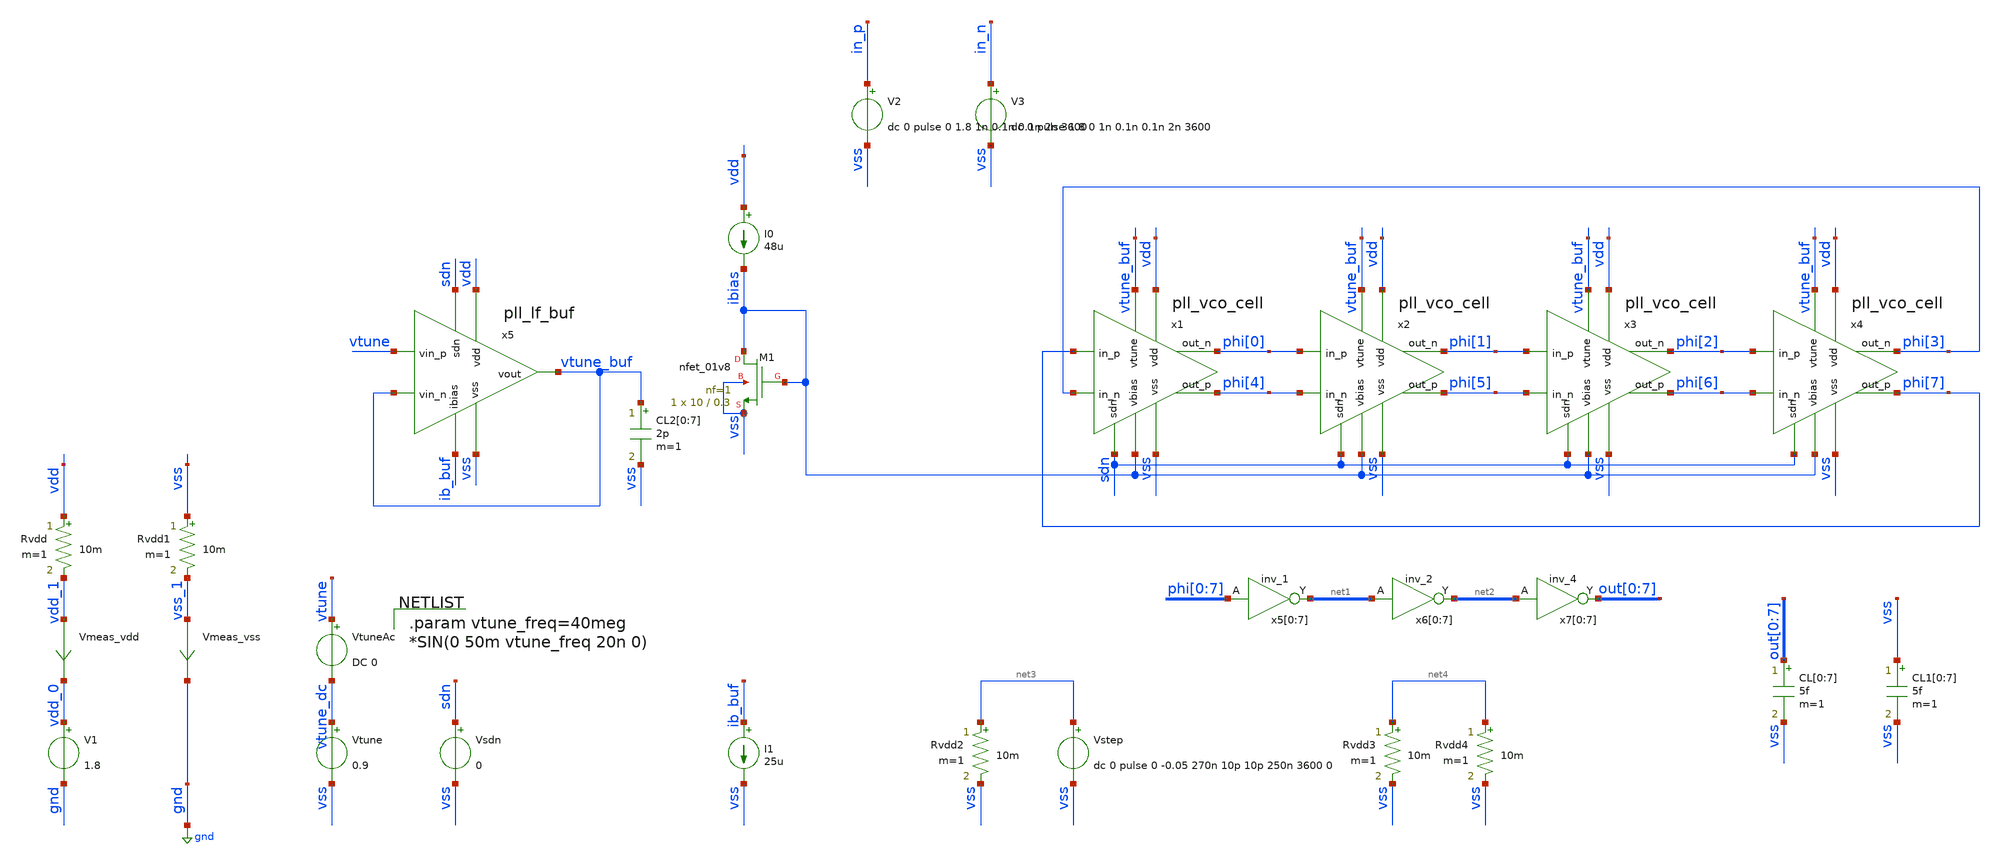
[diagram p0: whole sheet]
** sch_path: pll/pll_vco_cell/simulation/pll_vco_cell_tb.sch
**.subckt pll_vco_cell_tb
V1 vdd_0 gnd 1.8
I0 vdd ibias 48u
Vmeas_vdd vdd_1 vdd_0 0
.save i(vmeas_vdd)
Vtune vtune_dc vss 0.9
V2 in_p vss dc 0 pulse 0 1.8 1n 0.1n 0.1n 2n 3600
V3 in_n vss dc 0 pulse 1.8 0 1n 0.1n 0.1n 2n 3600
XM1 ibias ibias vss vss sky130_fd_pr__nfet_01v8 L=0.3 W=10 nf=1 ad='int((nf+1)/2) * W/nf * 0.29' as='int((nf+2)/2) * W/nf * 0.29'
+ pd='2*int((nf+1)/2) * (W/nf + 0.29)' ps='2*int((nf+2)/2) * (W/nf + 0.29)' nrd='0.29 / W' nrs='0.29 / W'
+ sa=0 sb=0 sd=0 mult=1 m=1
Vsdn sdn vss 0
x5[0] phi[0] vss vss vdd vdd net1[7] sky130_fd_sc_hs__inv_1
x5[1] phi[1] vss vss vdd vdd net1[6] sky130_fd_sc_hs__inv_1
x5[2] phi[2] vss vss vdd vdd net1[5] sky130_fd_sc_hs__inv_1
x5[3] phi[3] vss vss vdd vdd net1[4] sky130_fd_sc_hs__inv_1
x5[4] phi[4] vss vss vdd vdd net1[3] sky130_fd_sc_hs__inv_1
x5[5] phi[5] vss vss vdd vdd net1[2] sky130_fd_sc_hs__inv_1
x5[6] phi[6] vss vss vdd vdd net1[1] sky130_fd_sc_hs__inv_1
x5[7] phi[7] vss vss vdd vdd net1[0] sky130_fd_sc_hs__inv_1
x6[0] net1[7] vss vss vdd vdd net2[7] sky130_fd_sc_hs__inv_2
x6[1] net1[6] vss vss vdd vdd net2[6] sky130_fd_sc_hs__inv_2
x6[2] net1[5] vss vss vdd vdd net2[5] sky130_fd_sc_hs__inv_2
x6[3] net1[4] vss vss vdd vdd net2[4] sky130_fd_sc_hs__inv_2
x6[4] net1[3] vss vss vdd vdd net2[3] sky130_fd_sc_hs__inv_2
x6[5] net1[2] vss vss vdd vdd net2[2] sky130_fd_sc_hs__inv_2
x6[6] net1[1] vss vss vdd vdd net2[1] sky130_fd_sc_hs__inv_2
x6[7] net1[0] vss vss vdd vdd net2[0] sky130_fd_sc_hs__inv_2
x7[0] net2[7] vss vss vdd vdd out[0] sky130_fd_sc_hs__inv_4
x7[1] net2[6] vss vss vdd vdd out[1] sky130_fd_sc_hs__inv_4
x7[2] net2[5] vss vss vdd vdd out[2] sky130_fd_sc_hs__inv_4
x7[3] net2[4] vss vss vdd vdd out[3] sky130_fd_sc_hs__inv_4
x7[4] net2[3] vss vss vdd vdd out[4] sky130_fd_sc_hs__inv_4
x7[5] net2[2] vss vss vdd vdd out[5] sky130_fd_sc_hs__inv_4
x7[6] net2[1] vss vss vdd vdd out[6] sky130_fd_sc_hs__inv_4
x7[7] net2[0] vss vss vdd vdd out[7] sky130_fd_sc_hs__inv_4
CL[0] out[0] vss 5f m=1
CL[1] out[1] vss 5f m=1
CL[2] out[2] vss 5f m=1
CL[3] out[3] vss 5f m=1
CL[4] out[4] vss 5f m=1
CL[5] out[5] vss 5f m=1
CL[6] out[6] vss 5f m=1
CL[7] out[7] vss 5f m=1
Vmeas_vss vss_1 gnd 0
.save i(vmeas_vss)
Rvdd vdd vdd_1 10m m=1
Rvdd1 vss vss_1 10m m=1
CL1[0] vss vss 5f m=1
CL1[1] vss vss 5f m=1
CL1[2] vss vss 5f m=1
CL1[3] vss vss 5f m=1
CL1[4] vss vss 5f m=1
CL1[5] vss vss 5f m=1
CL1[6] vss vss 5f m=1
CL1[7] vss vss 5f m=1
VtuneAc vtune vtune_dc DC 0
Rvdd2 net3 vss 10m m=1
Vstep net3 vss dc 0 pulse 0 -0.05 270n 10p 10p 250n 3600 0
Rvdd3 net4 vss 10m m=1
Rvdd4 net4 vss 10m m=1
I1 ib_buf vss 25u
x1 phi[0] phi[4] phi[7] phi[3] vdd vtune_buf ibias vss sdn pll_vco_cell
x2 phi[1] phi[5] phi[0] phi[4] vdd vtune_buf ibias vss sdn pll_vco_cell
x3 phi[2] phi[6] phi[1] phi[5] vdd vtune_buf ibias vss sdn pll_vco_cell
x4 phi[3] phi[7] phi[2] phi[6] vdd vtune_buf ibias vss sdn pll_vco_cell
x5 vdd vtune sdn vtune_buf vtune_buf ib_buf vss pll_lf_buf
CL2[0] vtune_buf vss 2p m=1
CL2[1] vtune_buf vss 2p m=1
CL2[2] vtune_buf vss 2p m=1
CL2[3] vtune_buf vss 2p m=1
CL2[4] vtune_buf vss 2p m=1
CL2[5] vtune_buf vss 2p m=1
CL2[6] vtune_buf vss 2p m=1
CL2[7] vtune_buf vss 2p m=1
**** begin user architecture code



*.option savecurrents
*.option rshunt = 1e12
*.option gmin = 1e-24

** Settings for PSS osciallator
*.option reltol=1e-5
*.option vntol=3e-8
*.option abstol=1e-13
**.option chgtol=1e-12
*.option trtol=10
.option method=gear



* Set Oscillator nodes to initial conditions to start oscilation
*.ic v("phi<0>")=1.8 v("phi<4>")=0.0 v("phi<1>")=0.0 v("phi<5>")=1.8

.control

* #################################################################
* #
* #                         OPERATING POINT
* #
* #################################################################
reset
save all

* Bias transistor OP params
save i(@m.xm1.msky130_fd_pr__nfet_01v8[id])
save @m.xm1.msky130_fd_pr__nfet_01v8[gm]
save v(@m.xm1.msky130_fd_pr__nfet_01v8[vds])
save v(@m.xm1.msky130_fd_pr__nfet_01v8[vgs])
save v(@m.xm1.msky130_fd_pr__nfet_01v8[vth])
save v(@m.xm1.msky130_fd_pr__nfet_01v8[vdsat])

* VCO cell OP params
save i(@m.x1.xm1.msky130_fd_pr__nfet_01v8[id])
save @m.x1.xm1.msky130_fd_pr__nfet_01v8[gm]
save v(@m.x1.xm1.msky130_fd_pr__nfet_01v8[vds])
save v(@m.x1.xm1.msky130_fd_pr__nfet_01v8[vgs])
save v(@m.x1.xm1.msky130_fd_pr__nfet_01v8[vth])
save v(@m.x1.xm1.msky130_fd_pr__nfet_01v8[vdsat])

save i(@m.x1.xm2.msky130_fd_pr__nfet_01v8[id])
save @m.x1.xm2.msky130_fd_pr__nfet_01v8[gm]
save v(@m.x1.xm2.msky130_fd_pr__nfet_01v8[vds])
save v(@m.x1.xm2.msky130_fd_pr__nfet_01v8[vgs])
save v(@m.x1.xm2.msky130_fd_pr__nfet_01v8[vth])
save v(@m.x1.xm2.msky130_fd_pr__nfet_01v8[vdsat])

save i(@m.x1.xm3.msky130_fd_pr__nfet_01v8[id])
save @m.x1.xm3.msky130_fd_pr__nfet_01v8[gm]
save v(@m.x1.xm3.msky130_fd_pr__nfet_01v8[vds])
save v(@m.x1.xm3.msky130_fd_pr__nfet_01v8[vgs])
save v(@m.x1.xm3.msky130_fd_pr__nfet_01v8[vth])
save v(@m.x1.xm3.msky130_fd_pr__nfet_01v8[vdsat])

save i(@m.x1.xm4.msky130_fd_pr__pfet_01v8[id])
save @m.x1.xm4.msky130_fd_pr__pfet_01v8[gm]
save v(@m.x1.xm4.msky130_fd_pr__pfet_01v8[vds])
save v(@m.x1.xm4.msky130_fd_pr__pfet_01v8[vgs])
save v(@m.x1.xm4.msky130_fd_pr__pfet_01v8[vth])
save v(@m.x1.xm4.msky130_fd_pr__pfet_01v8[vdsat])

save i(@m.x1.xm5.msky130_fd_pr__pfet_01v8[id])
save @m.x1.xm5.msky130_fd_pr__pfet_01v8[gm]
save v(@m.x1.xm5.msky130_fd_pr__pfet_01v8[vds])
save v(@m.x1.xm5.msky130_fd_pr__pfet_01v8[vgs])
save v(@m.x1.xm5.msky130_fd_pr__pfet_01v8[vth])
save v(@m.x1.xm5.msky130_fd_pr__pfet_01v8[vdsat])

save i(@m.x1.xm6.msky130_fd_pr__pfet_01v8[id])
save @m.x1.xm6.msky130_fd_pr__pfet_01v8[gm]
save v(@m.x1.xm6.msky130_fd_pr__pfet_01v8[vds])
save v(@m.x1.xm6.msky130_fd_pr__pfet_01v8[vgs])
save v(@m.x1.xm6.msky130_fd_pr__pfet_01v8[vth])
save v(@m.x1.xm6.msky130_fd_pr__pfet_01v8[vdsat])

save i(@m.x1.xm7.msky130_fd_pr__pfet_01v8[id])
save @m.x1.xm7.msky130_fd_pr__pfet_01v8[gm]
save v(@m.x1.xm7.msky130_fd_pr__pfet_01v8[vds])
save v(@m.x1.xm7.msky130_fd_pr__pfet_01v8[vgs])
save v(@m.x1.xm7.msky130_fd_pr__pfet_01v8[vth])
save v(@m.x1.xm7.msky130_fd_pr__pfet_01v8[vdsat])


op
set filetype=binary
write pll_vco_cell_tb.raw all

* #################################################################
* #
* #                 TRANSIENT OSCILATION REGIME
* #
* #################################################################
reset
setplot const
save all
save v(in_p)
save v(in_n)
save v(vtune)
save v(vtune_buf)
save v(vsdn)

*ic v("phi<0>")=1.8 v("phi<4>")=0 v("phi<1>")=0 v("phi<5>")=1.8
tran 0.005n 500n uic
set filetype=ascii
write pll_vco_cell_tb_tran.raw v(vtune) v(vtune_buf) v("out<3>") v("out<7>") v("phi<3>") v("phi<7>")

* Plot internal nodes
*plot v("phi<0>") v("phi<4>")
*plot v("phi<1>") v("phi<5>")

* Plot outputs
plot v("out<0>")+2 v("out<4>")+2 v("out<1>")+0 v("out<5>")+0 v("out<2>")-2 v("out<6>")-2
+ v("out<3>")-4 v("out<7>")-4
plot v("phi<0>")+2 v("phi<4>")+2 v("phi<1>")+0 v("phi<5>")+0 v("phi<2>")-2 v("phi<6>")-2
+ v("phi<3>")-4 v("phi<7>")-4

*plot v("out<0>") v("out<4>")
*plot v("out<1>") v("out<5>")
*plot v("out<2>") v("out<6>")
*plot v("out<3>") v("out<7>")


* #################################################################
* #
* #                 TRANSIENT OSCILATION REGIME
* #
* #################################################################

let run_pss = 0
if run_pss > 0
	echo #############################################################
	echo Initial PSS run
	echo #############################################################

	reset
	setplot const
	save all

	*ic v("phi<0>")=1.8 v("phi<4>")=0 v("phi<1>")=0 v("phi<5>")=1.8
	pss 250e6 40n "out<7>" 128 10 3 100e-3 uic

	set filetype=ascii
	write pll_vco_cell_tb_pss.raw all
end

let run_pss_sweep = 0
if run_pss_sweep > 0
	echo #############################################################
	echo Sweep PSS run
	echo #############################################################

	reset
	setplot const
	save all

	let run = 0
	let vtune_start = 0.0
	let vtune_stop = 1.8
	let vtune_step = 0.01
	let vtune_val = vtune_start
	let vtune_length = (vtune_stop-vtune_start)/vtune_step

	set curplot = new
	set pss_sweep_plot = $curplot

	let fout = vector(vtune_length)
	let vtune_sweep = vector(vtune_length)

	while vtune_val le vtune_stop
		* Print run variables
		set run = $&run
		set run_total = $&vtune_length
		set vtune_val = $&vtune_val
		echo #############################################################
		echo PSS run: $run / $run_total for vtune: $vtune_val V
		echo #############################################################

		* Run Transient
		echo START TRAN
		set dt = $curplot
		reset

		* Set sweep variable
		alter Vtune = vtune_val
		echo 0: $vtune_val

		save vtune "v(out<7>)" "v(out<3>)"
		tran 0.005n 60n uic
		set filetype=ascii
		set tranfilename =  {pll_vco_cell_tb_tran_sweep_}{$&run}{.raw}
		echo $tranfilename
		write $tranfilename vtune "out<7>" "out<3>"
		echo END TRAN
		setplot $dt

		* Execute analysis + set plot environment
		echo START PSS
		reset

		* Set sweep variable
		alter Vtune = vtune_val
		echo Vtune DC: $vtune_val

		save vtune "v(out<7>)" "v(out<3>)"
		pss 200e6 40n "out<7>" 128 10 3 100e-3 uic
		set dt = $curplot
		setplot $pss_sweep_plot


		* Save values to variable
		let vtune_sweep[$run] = vtune_val
		let fout[$run] = {$dt}.frequency[1]

		let fosc=fout[$run]/1e6
		set fosc = $&fosc
		echo Measured Fosc: $fosc MHz

		echo END PSS
		setplot $dt

		let vtune_val = vtune_val + vtune_step
		let run = run + 1

	end
	*plot v({$pss_sweep_plot}.all)
	plot fout vs vtune_sweep

	setplot $pss_sweep_plot
	set filetype=ascii
	write pll_vco_cell_tb_pss_sweep.raw all
end

* #################################################################
* #
* #                 AC RESPONSE SIMULATED IN TRANSIENT
* #
* #################################################################

let run_tran_ac_sweep = 0
if run_tran_ac_sweep > 0
	echo #############################################################
	echo Sweep TRAN AC run
	echo #############################################################

	reset
	setplot const
	save all


	* Setup sweep values
	let vtune_freq_start = 100meg
	let vtune_freq_stop = 10000meg
	let vtune_freq_step = 100
	compose vtune_freq_vect dec=$&vtune_freq_step start=$&vtune_freq_start stop=$&vtune_freq_stop
	let vtune_freq_val = vtune_freq_vect[0]

	* Write frequency vector to file
	set filetype=ascii
	write pll_vco_cell_tb_tran_ac_sweep_input.raw vtune_freq_vect

	* Counter Values
	let run = 0
	let vtune_freq_length = 0
	foreach vtune_freq_val $&vtune_freq_vect
		let vtune_freq_length = vtune_freq_length + 1
	end

	* Setup Plot environment
	set curplot = new
	set tran_ac_sweep_plot = $curplot

	*let fout = vector(vtune_freq_length)
	*let vtune_freq_sweep = vector(vtune_freq_length)

	foreach vtune_freq_val $&vtune_freq_vect
		* Print run variables
		set run = $&run
		set run_total = $&vtune_freq_length
		echo #############################################################
		echo TRAN AC run: $run / $run_total for vtune: $vtune_freq_val Hz
		echo #############################################################

		* Run Transient
		echo START TRAN
		set dt = $curplot

		* Set sweep variable
		alterparam vtune_freq = $vtune_freq_val
		echo Vtune Frequency: $vtune_freq_val

		* Run
		reset
		save vtune vtune_buf "v(out<7>)" "v(out<3>)"
		tran 0.005n 520n uic
		set filetype=ascii
		set tranfilename =  {pll_vco_cell_tb_tran_ac_sweep_}{$&run}{.raw}
		echo $tranfilename
		write $tranfilename vtune "out<7>" "out<3>"
		echo END TRAN
		setplot $dt

		let run = run + 1
	end

	*setplot $pss_sweep_plot
	*set filetype=ascii
	*write pll_vco_cell_tb_pss_sweep.raw all
end


*rusage
.endc



.options wnflag=1
.include $::SKYWATER_MODELS/cells/nfet_01v8/sky130_fd_pr__nfet_01v8__tt.corner.spice
.include $::SKYWATER_MODELS/cells/nfet_01v8_lvt/sky130_fd_pr__nfet_01v8_lvt__tt.corner.spice
.include $::SKYWATER_MODELS/cells/pfet_01v8/sky130_fd_pr__pfet_01v8__tt.corner.spice
.include $::SKYWATER_MODELS/cells/nfet_03v3_nvt/sky130_fd_pr__nfet_03v3_nvt__tt.corner.spice
.include $::SKYWATER_MODELS/cells/nfet_05v0_nvt/sky130_fd_pr__nfet_05v0_nvt__tt.corner.spice
.include $::SKYWATER_MODELS/cells/esd_nfet_01v8/sky130_fd_pr__esd_nfet_01v8__tt.corner.spice
.include $::SKYWATER_MODELS/cells/pfet_01v8_lvt/sky130_fd_pr__pfet_01v8_lvt__tt.corner.spice
.include $::SKYWATER_MODELS/cells/pfet_01v8_hvt/sky130_fd_pr__pfet_01v8_hvt__tt.corner.spice
.include $::SKYWATER_MODELS/cells/esd_pfet_g5v0d10v5/sky130_fd_pr__esd_pfet_g5v0d10v5__tt.corner.spice
.include $::SKYWATER_MODELS/cells/pfet_g5v0d10v5/sky130_fd_pr__pfet_g5v0d10v5__tt.corner.spice
.include $::SKYWATER_MODELS/cells/pfet_g5v0d16v0/sky130_fd_pr__pfet_g5v0d16v0__tt.corner.spice
.include $::SKYWATER_MODELS/cells/nfet_g5v0d10v5/sky130_fd_pr__nfet_g5v0d10v5__tt.corner.spice
.include $::SKYWATER_MODELS/cells/nfet_g5v0d16v0/sky130_fd_pr__nfet_g5v0d16v0__tt_discrete.corner.spice
.include $::SKYWATER_MODELS/cells/esd_nfet_g5v0d10v5/sky130_fd_pr__esd_nfet_g5v0d10v5__tt.corner.spice
.include $::SKYWATER_MODELS/models/corners/tt/nonfet.spice

.include $::SKYWATER_MODELS/cells/cap_var_hvt/sky130_fd_pr__cap_var_hvt.model.spice

* Mismatch parameters
.include $::SKYWATER_MODELS/cells/nfet_01v8/sky130_fd_pr__nfet_01v8__mismatch.corner.spice
.include $::SKYWATER_MODELS/cells/pfet_01v8/sky130_fd_pr__pfet_01v8__mismatch.corner.spice
.include $::SKYWATER_MODELS/cells/nfet_01v8_lvt/sky130_fd_pr__nfet_01v8_lvt__mismatch.corner.spice
.include $::SKYWATER_MODELS/cells/pfet_01v8_lvt/sky130_fd_pr__pfet_01v8_lvt__mismatch.corner.spice
.include $::SKYWATER_MODELS/cells/pfet_01v8_hvt/sky130_fd_pr__pfet_01v8_hvt__mismatch.corner.spice
.include $::SKYWATER_MODELS/cells/nfet_g5v0d10v5/sky130_fd_pr__nfet_g5v0d10v5__mismatch.corner.spice
.include $::SKYWATER_MODELS/cells/pfet_g5v0d10v5/sky130_fd_pr__pfet_g5v0d10v5__mismatch.corner.spice
.include $::SKYWATER_MODELS/cells/nfet_05v0_nvt/sky130_fd_pr__nfet_05v0_nvt__mismatch.corner.spice
.include $::SKYWATER_MODELS/cells/nfet_03v3_nvt/sky130_fd_pr__nfet_03v3_nvt__mismatch.corner.spice

* Resistor$::SKYWATER_MODELS/Capacitor
.include $::SKYWATER_MODELS/models/r+c/res_typical__cap_typical.spice
.include $::SKYWATER_MODELS/models/r+c/res_typical__cap_typical__lin.spice

* Special cells
.include $::SKYWATER_MODELS/models/corners/tt/specialized_cells.spice

* All models
.include $::SKYWATER_MODELS/models/all.spice

* Corner
.include $::SKYWATER_MODELS/models/corners/tt/rf.spice

* .include $::SKYWATER_STDCELLS/cells/
.include $::SKYWATER_STDCELLS/cells/buf/sky130_fd_sc_hd__buf_1.spice
.include $::SKYWATER_STDCELLS_HS/cells/buf/sky130_fd_sc_hs__buf_1.spice
.include $::SKYWATER_STDCELLS_HS/cells/buf/sky130_fd_sc_hs__buf_16.spice
.include $::SKYWATER_STDCELLS/cells/clkbuf/sky130_fd_sc_hd__clkbuf_1.spice
.include $::SKYWATER_STDCELLS/cells/clkbuf/sky130_fd_sc_hd__clkbuf_2.spice
.include $::SKYWATER_STDCELLS/cells/clkbuf/sky130_fd_sc_hd__clkbuf_4.spice
.include $::SKYWATER_STDCELLS/cells/clkbuf/sky130_fd_sc_hd__clkbuf_8.spice
.include $::SKYWATER_STDCELLS/cells/clkbuf/sky130_fd_sc_hd__clkbuf_16.spice
.include $::SKYWATER_STDCELLS/cells/decap/sky130_fd_sc_hd__decap_3.spice
.include $::SKYWATER_STDCELLS/cells/decap/sky130_fd_sc_hd__decap_4.spice
.include $::SKYWATER_STDCELLS/cells/decap/sky130_fd_sc_hd__decap_8.spice
.include $::SKYWATER_STDCELLS/cells/dfrbp/sky130_fd_sc_hd__dfrbp_1.spice
.include $::SKYWATER_STDCELLS/cells/dfrbp/sky130_fd_sc_hd__dfrbp_2.spice
.include $::SKYWATER_STDCELLS/cells/inv/sky130_fd_sc_hd__inv_1.spice
.include $::SKYWATER_STDCELLS/cells/inv/sky130_fd_sc_hd__inv_2.spice
.include $::SKYWATER_STDCELLS/cells/inv/sky130_fd_sc_hd__inv_4.spice
.include $::SKYWATER_STDCELLS/cells/inv/sky130_fd_sc_hd__inv_8.spice
.include $::SKYWATER_STDCELLS/cells/inv/sky130_fd_sc_hd__inv_16.spice
.include $::SKYWATER_STDCELLS_HS/cells/inv/sky130_fd_sc_hs__inv_1.spice
.include $::SKYWATER_STDCELLS_HS/cells/inv/sky130_fd_sc_hs__inv_2.spice
.include $::SKYWATER_STDCELLS_HS/cells/inv/sky130_fd_sc_hs__inv_4.spice
.include $::SKYWATER_STDCELLS_HS/cells/inv/sky130_fd_sc_hs__inv_8.spice
.include $::SKYWATER_STDCELLS_HS/cells/inv/sky130_fd_sc_hs__inv_16.spice
.include $::SKYWATER_STDCELLS/cells/mux2/sky130_fd_sc_hd__mux2_2.spice
.include $::SKYWATER_STDCELLS/cells/nand2/sky130_fd_sc_hd__nand2_1.spice
.include $::SKYWATER_STDCELLS/cells/tap/sky130_fd_sc_hd__tap_2.spice
.include $::SKYWATER_STDCELLS/cells/tapvpwrvgnd/sky130_fd_sc_hd__tapvpwrvgnd_1.spice


.param vtune_freq=40meg
*SIN(0 50m vtune_freq 20n 0)


**** end user architecture code
**.ends

* expanding   symbol:  test_jens/pll/pll_vco/pll_vco_cell.sym # of pins=9
** sym_path: pll/pll_vco_cell/xschem/pll_vco_cell.sym
** sch_path: pll/pll_vco_cell/xschem/pll_vco_cell.sch
.subckt pll_vco_cell out_n out_p in_p in_n vdd vtune vbias vss sdn
*.iopin vss
*.iopin vdd
*.ipin in_p
*.ipin in_n
*.iopin vbias
*.opin out_n
*.opin out_p
*.ipin vtune
*.ipin sdn
**** begin user architecture code


*.control
*save i(@m.${path}xm1.msky130_fd_pr__nfet_01v8[id])
*save @m.${path}xm1.msky130_fd_pr__nfet_01v8[gm]
*save v(@m.${path}xm1.msky130_fd_pr__nfet_01v8[vds])
*save v(@m.${path}xm1.msky130_fd_pr__nfet_01v8[vgs])
*save v(@m.${path}xm1.msky130_fd_pr__nfet_01v8[vth])
*save v(@m.${path}xm1.msky130_fd_pr__nfet_01v8[vdsat])

*save i(@m.${path}xm2.msky130_fd_pr__nfet_01v8[id])
*save @m.${path}xm2.msky130_fd_pr__nfet_01v8[gm]
*save v(@m.${path}xm2.msky130_fd_pr__nfet_01v8[vds])
*save v(@m.${path}xm2.msky130_fd_pr__nfet_01v8[vgs])
*save v(@m.${path}xm2.msky130_fd_pr__nfet_01v8[vth])
*save v(@m.${path}xm2.msky130_fd_pr__nfet_01v8[vdsat])
*.endc


**** end user architecture code
XM3 net1 vbias vss vss sky130_fd_pr__nfet_01v8 L=0.3 W=60 nf=1 ad='int((nf+1)/2) * W/nf * 0.29' as='int((nf+2)/2) * W/nf * 0.29'
+ pd='2*int((nf+1)/2) * (W/nf + 0.29)' ps='2*int((nf+2)/2) * (W/nf + 0.29)' nrd='0.29 / W' nrs='0.29 / W'
+ sa=0 sb=0 sd=0 mult=4 m=4
XM10 vbias sdn vss vss sky130_fd_pr__nfet_01v8 L=0.15 W=0.5 nf=1 ad='int((nf+1)/2) * W/nf * 0.29' as='int((nf+2)/2) * W/nf * 0.29'
+ pd='2*int((nf+1)/2) * (W/nf + 0.29)' ps='2*int((nf+2)/2) * (W/nf + 0.29)' nrd='0.29 / W' nrs='0.29 / W'
+ sa=0 sb=0 sd=0 mult=1 m=1
x1 sdn vss vss vdd vdd net2 sky130_fd_sc_hd__inv_1
x2 sdn vss vss vdd vdd net3 sky130_fd_sc_hd__inv_1
XM4 out_n out_n vdd vdd sky130_fd_pr__pfet_01v8 L=0.15 W=8 nf=1 ad='int((nf+1)/2) * W/nf * 0.29' as='int((nf+2)/2) * W/nf * 0.29'
+ pd='2*int((nf+1)/2) * (W/nf + 0.29)' ps='2*int((nf+2)/2) * (W/nf + 0.29)' nrd='0.29 / W' nrs='0.29 / W'
+ sa=0 sb=0 sd=0 mult=1 m=1
XM5 out_p out_p vdd vdd sky130_fd_pr__pfet_01v8 L=0.15 W=8 nf=1 ad='int((nf+1)/2) * W/nf * 0.29' as='int((nf+2)/2) * W/nf * 0.29'
+ pd='2*int((nf+1)/2) * (W/nf + 0.29)' ps='2*int((nf+2)/2) * (W/nf + 0.29)' nrd='0.29 / W' nrs='0.29 / W'
+ sa=0 sb=0 sd=0 mult=1 m=1
XM7 out_p out_n vdd vdd sky130_fd_pr__pfet_01v8 L=0.15 W=16 nf=1 ad='int((nf+1)/2) * W/nf * 0.29' as='int((nf+2)/2) * W/nf * 0.29'
+ pd='2*int((nf+1)/2) * (W/nf + 0.29)' ps='2*int((nf+2)/2) * (W/nf + 0.29)' nrd='0.29 / W' nrs='0.29 / W'
+ sa=0 sb=0 sd=0 mult=1 m=1
XM6 out_n out_p vdd vdd sky130_fd_pr__pfet_01v8 L=0.15 W=16 nf=1 ad='int((nf+1)/2) * W/nf * 0.29' as='int((nf+2)/2) * W/nf * 0.29'
+ pd='2*int((nf+1)/2) * (W/nf + 0.29)' ps='2*int((nf+2)/2) * (W/nf + 0.29)' nrd='0.29 / W' nrs='0.29 / W'
+ sa=0 sb=0 sd=0 mult=1 m=1
XM8 out_n net2 vdd vdd sky130_fd_pr__pfet_01v8 L=0.15 W=0.5 nf=1 ad='int((nf+1)/2) * W/nf * 0.29' as='int((nf+2)/2) * W/nf * 0.29'
+ pd='2*int((nf+1)/2) * (W/nf + 0.29)' ps='2*int((nf+2)/2) * (W/nf + 0.29)' nrd='0.29 / W' nrs='0.29 / W'
+ sa=0 sb=0 sd=0 mult=1 m=1
XM9 out_p net3 vdd vdd sky130_fd_pr__pfet_01v8 L=0.15 W=0.5 nf=1 ad='int((nf+1)/2) * W/nf * 0.29' as='int((nf+2)/2) * W/nf * 0.29'
+ pd='2*int((nf+1)/2) * (W/nf + 0.29)' ps='2*int((nf+2)/2) * (W/nf + 0.29)' nrd='0.29 / W' nrs='0.29 / W'
+ sa=0 sb=0 sd=0 mult=1 m=1
XM1 out_n in_p net1 vss sky130_fd_pr__nfet_01v8 L=0.15 W=16 nf=1 ad='int((nf+1)/2) * W/nf * 0.29' as='int((nf+2)/2) * W/nf * 0.29'
+ pd='2*int((nf+1)/2) * (W/nf + 0.29)' ps='2*int((nf+2)/2) * (W/nf + 0.29)' nrd='0.29 / W' nrs='0.29 / W'
+ sa=0 sb=0 sd=0 mult=1 m=1
XM2 out_p in_n net1 vss sky130_fd_pr__nfet_01v8 L=0.15 W=16 nf=1 ad='int((nf+1)/2) * W/nf * 0.29' as='int((nf+2)/2) * W/nf * 0.29'
+ pd='2*int((nf+1)/2) * (W/nf + 0.29)' ps='2*int((nf+2)/2) * (W/nf + 0.29)' nrd='0.29 / W' nrs='0.29 / W'
+ sa=0 sb=0 sd=0 mult=1 m=1
XC1 out_n vtune vss sky130_fd_pr__cap_var_lvt W=7 L=4 VM=3 m=3
XC2 out_p vtune vss sky130_fd_pr__cap_var_lvt W=7 L=4 VM=3 m=3
.ends


* expanding   symbol:  test_jens/pll/pll_lf_buf/pll_lf_buf.sym # of pins=7
** sym_path: pll/pll_lf_buf/xschem/pll_lf_buf.sym
** sch_path: pll/pll_lf_buf/xschem/pll_lf_buf.sch
.subckt pll_lf_buf vdd vin_p sdn vin_n vout ibias vss
*.iopin vss
*.iopin vdd
*.ipin vin_p
*.ipin vin_n
*.iopin ibias
*.opin vout
*.ipin sdn
XM1 net4 vin_p net1 vdd sky130_fd_pr__pfet_01v8 L=0.15 W=16 nf=2 ad='int((nf+1)/2) * W/nf * 0.29' as='int((nf+2)/2) * W/nf * 0.29'
+ pd='2*int((nf+1)/2) * (W/nf + 0.29)' ps='2*int((nf+2)/2) * (W/nf + 0.29)' nrd='0.29 / W' nrs='0.29 / W'
+ sa=0 sb=0 sd=0 mult=8 m=8
XM2 net5 vin_n net1 vdd sky130_fd_pr__pfet_01v8 L=0.15 W=16 nf=2 ad='int((nf+1)/2) * W/nf * 0.29' as='int((nf+2)/2) * W/nf * 0.29'
+ pd='2*int((nf+1)/2) * (W/nf + 0.29)' ps='2*int((nf+2)/2) * (W/nf + 0.29)' nrd='0.29 / W' nrs='0.29 / W'
+ sa=0 sb=0 sd=0 mult=8 m=8
XM3 vbn vbp_casc net2 vdd sky130_fd_pr__pfet_01v8 L=0.3 W=16 nf=2 ad='int((nf+1)/2) * W/nf * 0.29' as='int((nf+2)/2) * W/nf * 0.29'
+ pd='2*int((nf+1)/2) * (W/nf + 0.29)' ps='2*int((nf+2)/2) * (W/nf + 0.29)' nrd='0.29 / W' nrs='0.29 / W'
+ sa=0 sb=0 sd=0 mult=8 m=8
XM4 vout vbp_casc net3 vdd sky130_fd_pr__pfet_01v8 L=0.3 W=16 nf=2 ad='int((nf+1)/2) * W/nf * 0.29' as='int((nf+2)/2) * W/nf * 0.29'
+ pd='2*int((nf+1)/2) * (W/nf + 0.29)' ps='2*int((nf+2)/2) * (W/nf + 0.29)' nrd='0.29 / W' nrs='0.29 / W'
+ sa=0 sb=0 sd=0 mult=8 m=8
XM5 net2 vbp vdd vdd sky130_fd_pr__pfet_01v8 L=0.3 W=16 nf=2 ad='int((nf+1)/2) * W/nf * 0.29' as='int((nf+2)/2) * W/nf * 0.29'
+ pd='2*int((nf+1)/2) * (W/nf + 0.29)' ps='2*int((nf+2)/2) * (W/nf + 0.29)' nrd='0.29 / W' nrs='0.29 / W'
+ sa=0 sb=0 sd=0 mult=8 m=8
XM6 net3 vbp vdd vdd sky130_fd_pr__pfet_01v8 L=0.3 W=16 nf=2 ad='int((nf+1)/2) * W/nf * 0.29' as='int((nf+2)/2) * W/nf * 0.29'
+ pd='2*int((nf+1)/2) * (W/nf + 0.29)' ps='2*int((nf+2)/2) * (W/nf + 0.29)' nrd='0.29 / W' nrs='0.29 / W'
+ sa=0 sb=0 sd=0 mult=8 m=8
XM7 vbn vbn_casc net4 vss sky130_fd_pr__nfet_01v8 L=0.3 W=8 nf=2 ad='int((nf+1)/2) * W/nf * 0.29' as='int((nf+2)/2) * W/nf * 0.29'
+ pd='2*int((nf+1)/2) * (W/nf + 0.29)' ps='2*int((nf+2)/2) * (W/nf + 0.29)' nrd='0.29 / W' nrs='0.29 / W'
+ sa=0 sb=0 sd=0 mult=8 m=8
XM8 vout vbn_casc net5 vss sky130_fd_pr__nfet_01v8 L=0.3 W=8 nf=2 ad='int((nf+1)/2) * W/nf * 0.29' as='int((nf+2)/2) * W/nf * 0.29'
+ pd='2*int((nf+1)/2) * (W/nf + 0.29)' ps='2*int((nf+2)/2) * (W/nf + 0.29)' nrd='0.29 / W' nrs='0.29 / W'
+ sa=0 sb=0 sd=0 mult=8 m=8
XM9 net4 vbn vss vss sky130_fd_pr__nfet_01v8 L=0.3 W=8 nf=2 ad='int((nf+1)/2) * W/nf * 0.29' as='int((nf+2)/2) * W/nf * 0.29'
+ pd='2*int((nf+1)/2) * (W/nf + 0.29)' ps='2*int((nf+2)/2) * (W/nf + 0.29)' nrd='0.29 / W' nrs='0.29 / W'
+ sa=0 sb=0 sd=0 mult=8 m=8
XM10 net5 vbn vss vss sky130_fd_pr__nfet_01v8 L=0.3 W=8 nf=2 ad='int((nf+1)/2) * W/nf * 0.29' as='int((nf+2)/2) * W/nf * 0.29'
+ pd='2*int((nf+1)/2) * (W/nf + 0.29)' ps='2*int((nf+2)/2) * (W/nf + 0.29)' nrd='0.29 / W' nrs='0.29 / W'
+ sa=0 sb=0 sd=0 mult=8 m=8
XM11 net1 vbp vdd vdd sky130_fd_pr__pfet_01v8 L=0.3 W=8 nf=2 ad='int((nf+1)/2) * W/nf * 0.29' as='int((nf+2)/2) * W/nf * 0.29'
+ pd='2*int((nf+1)/2) * (W/nf + 0.29)' ps='2*int((nf+2)/2) * (W/nf + 0.29)' nrd='0.29 / W' nrs='0.29 / W'
+ sa=0 sb=0 sd=0 mult=8 m=8
XM12 net9 net10 vdd vdd sky130_fd_pr__pfet_01v8 L=0.3 W=16 nf=2 ad='int((nf+1)/2) * W/nf * 0.29' as='int((nf+2)/2) * W/nf * 0.29'
+ pd='2*int((nf+1)/2) * (W/nf + 0.29)' ps='2*int((nf+2)/2) * (W/nf + 0.29)' nrd='0.29 / W' nrs='0.29 / W'
+ sa=0 sb=0 sd=0 mult=1 m=1
XM13 net6 vbp vdd vdd sky130_fd_pr__pfet_01v8 L=0.3 W=16 nf=2 ad='int((nf+1)/2) * W/nf * 0.29' as='int((nf+2)/2) * W/nf * 0.29'
+ pd='2*int((nf+1)/2) * (W/nf + 0.29)' ps='2*int((nf+2)/2) * (W/nf + 0.29)' nrd='0.29 / W' nrs='0.29 / W'
+ sa=0 sb=0 sd=0 mult=1 m=1
XM14 net10 net8 net9 vdd sky130_fd_pr__pfet_01v8 L=0.3 W=16 nf=2 ad='int((nf+1)/2) * W/nf * 0.29' as='int((nf+2)/2) * W/nf * 0.29'
+ pd='2*int((nf+1)/2) * (W/nf + 0.29)' ps='2*int((nf+2)/2) * (W/nf + 0.29)' nrd='0.29 / W' nrs='0.29 / W'
+ sa=0 sb=0 sd=0 mult=1 m=1
XM15 vbn_casc vbp_casc net6 vdd sky130_fd_pr__pfet_01v8 L=0.3 W=16 nf=2 ad='int((nf+1)/2) * W/nf * 0.29'
+ as='int((nf+2)/2) * W/nf * 0.29' pd='2*int((nf+1)/2) * (W/nf + 0.29)' ps='2*int((nf+2)/2) * (W/nf + 0.29)'
+ nrd='0.29 / W' nrs='0.29 / W' sa=0 sb=0 sd=0 mult=1 m=1
XM16 vbn_casc vbn_casc vss vss sky130_fd_pr__nfet_01v8 L=1.2 W=4 nf=2 ad='int((nf+1)/2) * W/nf * 0.29'
+ as='int((nf+2)/2) * W/nf * 0.29' pd='2*int((nf+1)/2) * (W/nf + 0.29)' ps='2*int((nf+2)/2) * (W/nf + 0.29)'
+ nrd='0.29 / W' nrs='0.29 / W' sa=0 sb=0 sd=0 mult=1 m=1
XM17 net7 vbn_casc vss vss sky130_fd_pr__nfet_01v8 L=1.2 W=4 nf=2 ad='int((nf+1)/2) * W/nf * 0.29' as='int((nf+2)/2) * W/nf * 0.29'
+ pd='2*int((nf+1)/2) * (W/nf + 0.29)' ps='2*int((nf+2)/2) * (W/nf + 0.29)' nrd='0.29 / W' nrs='0.29 / W'
+ sa=0 sb=0 sd=0 mult=1 m=1
XM18 net7 net7 vdd vdd sky130_fd_pr__pfet_01v8 L=1.2 W=16 nf=2 ad='int((nf+1)/2) * W/nf * 0.29' as='int((nf+2)/2) * W/nf * 0.29'
+ pd='2*int((nf+1)/2) * (W/nf + 0.29)' ps='2*int((nf+2)/2) * (W/nf + 0.29)' nrd='0.29 / W' nrs='0.29 / W'
+ sa=0 sb=0 sd=0 mult=1 m=1
XM19 vbn sdn vss vss sky130_fd_pr__nfet_01v8 L=0.3 W=1 nf=1 ad='int((nf+1)/2) * W/nf * 0.29' as='int((nf+2)/2) * W/nf * 0.29'
+ pd='2*int((nf+1)/2) * (W/nf + 0.29)' ps='2*int((nf+2)/2) * (W/nf + 0.29)' nrd='0.29 / W' nrs='0.29 / W'
+ sa=0 sb=0 sd=0 mult=1 m=1
XM20 vbn_casc sdn vss vss sky130_fd_pr__nfet_01v8 L=0.3 W=1 nf=1 ad='int((nf+1)/2) * W/nf * 0.29' as='int((nf+2)/2) * W/nf * 0.29'
+ pd='2*int((nf+1)/2) * (W/nf + 0.29)' ps='2*int((nf+2)/2) * (W/nf + 0.29)' nrd='0.29 / W' nrs='0.29 / W'
+ sa=0 sb=0 sd=0 mult=1 m=1
XM21 vbp sdn_b vdd vdd sky130_fd_pr__pfet_01v8 L=0.3 W=1 nf=1 ad='int((nf+1)/2) * W/nf * 0.29' as='int((nf+2)/2) * W/nf * 0.29'
+ pd='2*int((nf+1)/2) * (W/nf + 0.29)' ps='2*int((nf+2)/2) * (W/nf + 0.29)' nrd='0.29 / W' nrs='0.29 / W'
+ sa=0 sb=0 sd=0 mult=1 m=1
XM22 vbp_casc sdn_b vdd vdd sky130_fd_pr__pfet_01v8 L=0.3 W=1 nf=1 ad='int((nf+1)/2) * W/nf * 0.29' as='int((nf+2)/2) * W/nf * 0.29'
+ pd='2*int((nf+1)/2) * (W/nf + 0.29)' ps='2*int((nf+2)/2) * (W/nf + 0.29)' nrd='0.29 / W' nrs='0.29 / W'
+ sa=0 sb=0 sd=0 mult=1 m=1
XM23 net8 sdn_b ibias vss sky130_fd_pr__nfet_01v8 L=0.15 W=4 nf=8 ad='int((nf+1)/2) * W/nf * 0.29' as='int((nf+2)/2) * W/nf * 0.29'
+ pd='2*int((nf+1)/2) * (W/nf + 0.29)' ps='2*int((nf+2)/2) * (W/nf + 0.29)' nrd='0.29 / W' nrs='0.29 / W'
+ sa=0 sb=0 sd=0 mult=1 m=1
**** begin user architecture code

.include $::SKYWATER_STDCELLS/cells/inv/sky130_fd_sc_hd__inv_1.spice
.include $::SKYWATER_STDCELLS/cells/inv/sky130_fd_sc_hd__inv_2.spice
.include $::SKYWATER_STDCELLS/cells/inv/sky130_fd_sc_hd__inv_4.spice
.include $::SKYWATER_STDCELLS/cells/inv/sky130_fd_sc_hd__inv_8.spice

**** end user architecture code
x1 sdn vss vss vdd vdd sdn_b sky130_fd_sc_hd__inv_1
R1 net10 net8 8k m=1
R2 vbp_casc net8 1 m=1
R3 vbp net10 1 m=1
XM24 ibias sdn net8 vdd sky130_fd_pr__pfet_01v8 L=0.15 W=12 nf=8 ad='int((nf+1)/2) * W/nf * 0.29' as='int((nf+2)/2) * W/nf * 0.29'
+ pd='2*int((nf+1)/2) * (W/nf + 0.29)' ps='2*int((nf+2)/2) * (W/nf + 0.29)' nrd='0.29 / W' nrs='0.29 / W'
+ sa=0 sb=0 sd=0 mult=1 m=1
.ends

.GLOBAL gnd
.end
